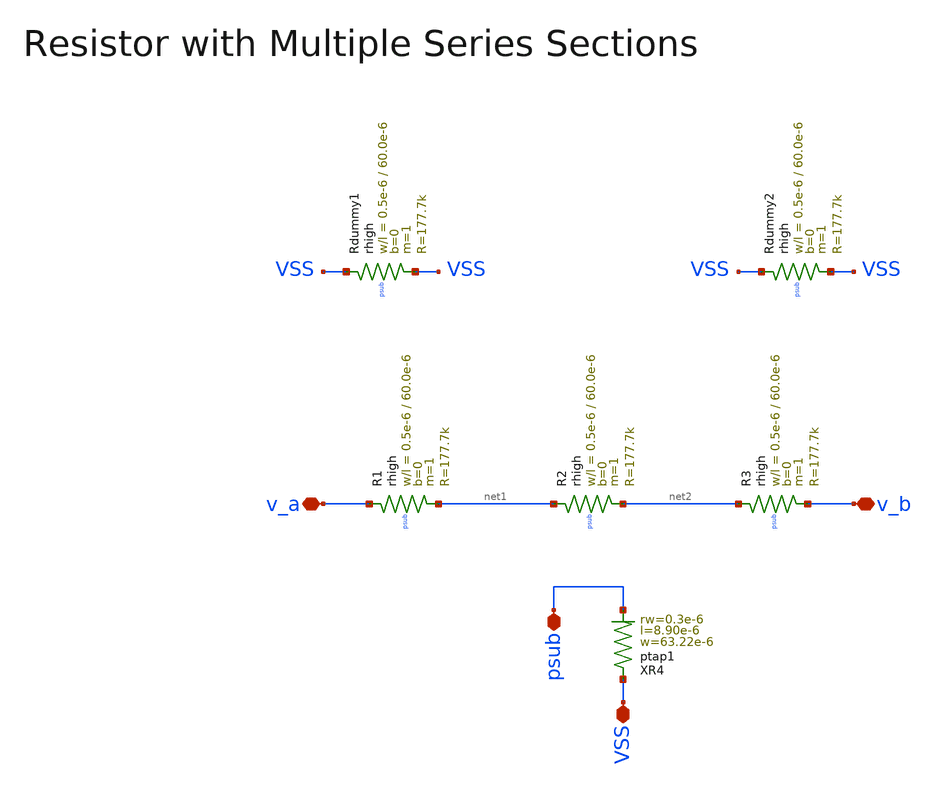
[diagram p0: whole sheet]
** sch_path: ihp130/macros/iqmod/schematic/iqmod_mfb_lpf_R4.sch
**.subckt iqmod_mfb_lpf_R4 v_a v_b VSS psub
*.iopin v_a
*.iopin v_b
*.iopin VSS
*.iopin psub
XR1 v_a net1 psub rhigh w=0.5e-6 l=60.0e-6 m=1 b=0 mm_ok=1
XR2 net1 net2 psub rhigh w=0.5e-6 l=60.0e-6 m=1 b=0 mm_ok=1
XR3 net2 v_b psub rhigh w=0.5e-6 l=60.0e-6 m=1 b=0 mm_ok=1
XRdummy1 VSS VSS psub rhigh w=0.5e-6 l=60.0e-6 m=1 b=0 mm_ok=1
XRdummy2 VSS VSS psub rhigh w=0.5e-6 l=60.0e-6 m=1 b=0 mm_ok=1
XR4 VSS psub ptap1 R=1.593 w=63.22e-6 l=8.90e-6 rw=0.3e-6
**.ends
.end
